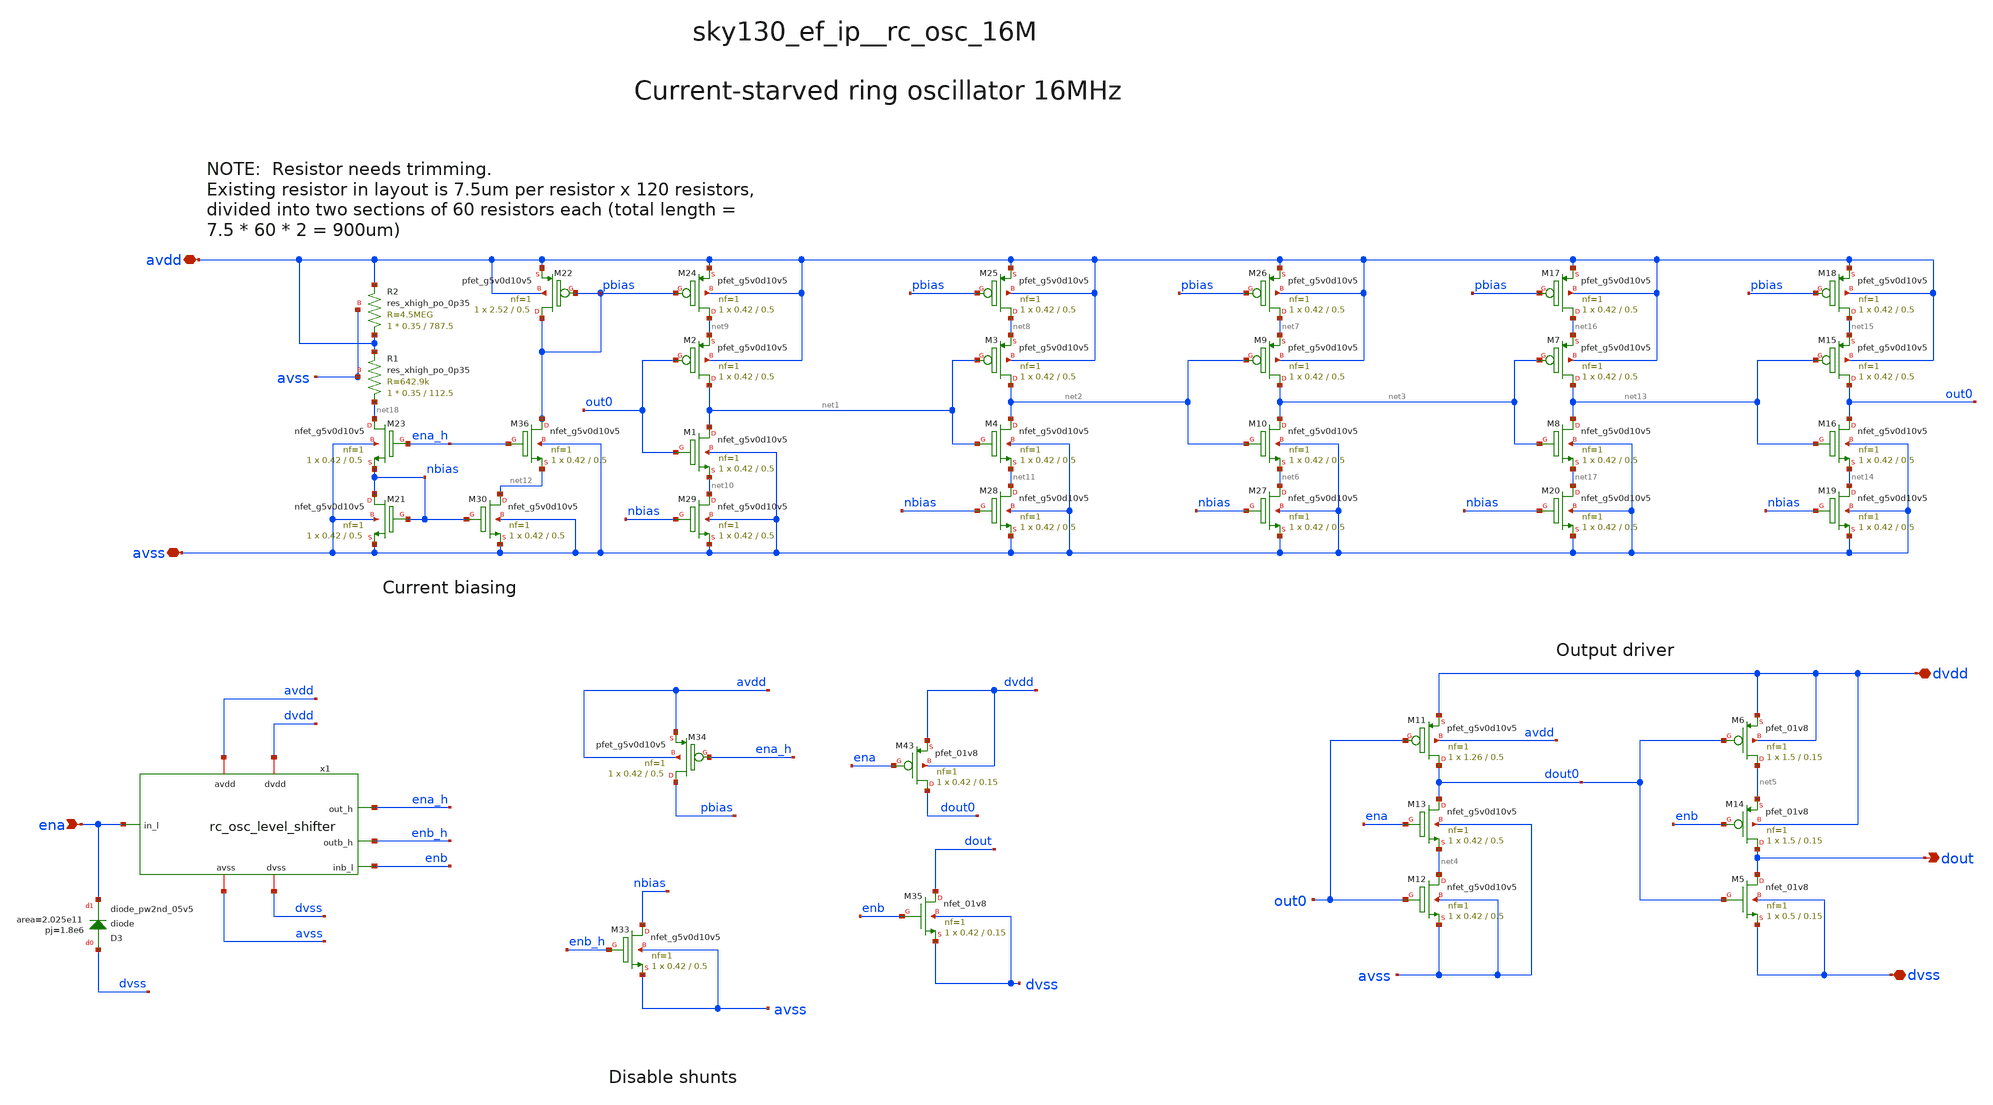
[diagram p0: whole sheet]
** sch_path: xschem/sky130_ef_ip__rc_osc_16M.sch
**.subckt sky130_ef_ip__rc_osc_16M avdd avss dvss dvdd ena dout
*.iopin avdd
*.iopin avss
*.iopin dvss
*.iopin dvdd
*.ipin ena
*.opin dout
XM1 net1 out0 net10 avss sky130_fd_pr__nfet_g5v0d10v5 L=0.5 W=0.42 nf=1 ad='int((nf+1)/2) * W/nf * 0.29'
+ as='int((nf+2)/2) * W/nf * 0.29' pd='2*int((nf+1)/2) * (W/nf + 0.29)' ps='2*int((nf+2)/2) * (W/nf + 0.29)'
+ nrd='0.29 / W' nrs='0.29 / W' sa=0 sb=0 sd=0 mult=1 m=1
XM2 net1 out0 net9 avdd sky130_fd_pr__pfet_g5v0d10v5 L=0.5 W=0.42 nf=1 ad='int((nf+1)/2) * W/nf * 0.29'
+ as='int((nf+2)/2) * W/nf * 0.29' pd='2*int((nf+1)/2) * (W/nf + 0.29)' ps='2*int((nf+2)/2) * (W/nf + 0.29)'
+ nrd='0.29 / W' nrs='0.29 / W' sa=0 sb=0 sd=0 mult=1 m=1
XM3 net2 net1 net8 avdd sky130_fd_pr__pfet_g5v0d10v5 L=0.5 W=0.42 nf=1 ad='int((nf+1)/2) * W/nf * 0.29'
+ as='int((nf+2)/2) * W/nf * 0.29' pd='2*int((nf+1)/2) * (W/nf + 0.29)' ps='2*int((nf+2)/2) * (W/nf + 0.29)'
+ nrd='0.29 / W' nrs='0.29 / W' sa=0 sb=0 sd=0 mult=1 m=1
XM4 net2 net1 net11 avss sky130_fd_pr__nfet_g5v0d10v5 L=0.5 W=0.42 nf=1 ad='int((nf+1)/2) * W/nf * 0.29'
+ as='int((nf+2)/2) * W/nf * 0.29' pd='2*int((nf+1)/2) * (W/nf + 0.29)' ps='2*int((nf+2)/2) * (W/nf + 0.29)'
+ nrd='0.29 / W' nrs='0.29 / W' sa=0 sb=0 sd=0 mult=1 m=1
XM5 dout dout0 dvss dvss sky130_fd_pr__nfet_01v8 L=0.15 W=0.5 nf=1 ad='int((nf+1)/2) * W/nf * 0.29' as='int((nf+2)/2) * W/nf * 0.29'
+ pd='2*int((nf+1)/2) * (W/nf + 0.29)' ps='2*int((nf+2)/2) * (W/nf + 0.29)' nrd='0.29 / W' nrs='0.29 / W'
+ sa=0 sb=0 sd=0 mult=1 m=1
XM6 net5 dout0 dvdd dvdd sky130_fd_pr__pfet_01v8 L=0.15 W=1.5 nf=1 ad='int((nf+1)/2) * W/nf * 0.29' as='int((nf+2)/2) * W/nf * 0.29'
+ pd='2*int((nf+1)/2) * (W/nf + 0.29)' ps='2*int((nf+2)/2) * (W/nf + 0.29)' nrd='0.29 / W' nrs='0.29 / W'
+ sa=0 sb=0 sd=0 mult=1 m=1
XM9 net3 net2 net7 avdd sky130_fd_pr__pfet_g5v0d10v5 L=0.5 W=0.42 nf=1 ad='int((nf+1)/2) * W/nf * 0.29'
+ as='int((nf+2)/2) * W/nf * 0.29' pd='2*int((nf+1)/2) * (W/nf + 0.29)' ps='2*int((nf+2)/2) * (W/nf + 0.29)'
+ nrd='0.29 / W' nrs='0.29 / W' sa=0 sb=0 sd=0 mult=1 m=1
XM10 net3 net2 net6 avss sky130_fd_pr__nfet_g5v0d10v5 L=0.5 W=0.42 nf=1 ad='int((nf+1)/2) * W/nf * 0.29'
+ as='int((nf+2)/2) * W/nf * 0.29' pd='2*int((nf+1)/2) * (W/nf + 0.29)' ps='2*int((nf+2)/2) * (W/nf + 0.29)'
+ nrd='0.29 / W' nrs='0.29 / W' sa=0 sb=0 sd=0 mult=1 m=1
XM11 dout0 out0 dvdd avdd sky130_fd_pr__pfet_g5v0d10v5 L=0.5 W=1.26 nf=1 ad='int((nf+1)/2) * W/nf * 0.29'
+ as='int((nf+2)/2) * W/nf * 0.29' pd='2*int((nf+1)/2) * (W/nf + 0.29)' ps='2*int((nf+2)/2) * (W/nf + 0.29)'
+ nrd='0.29 / W' nrs='0.29 / W' sa=0 sb=0 sd=0 mult=1 m=1
XM12 net4 out0 avss avss sky130_fd_pr__nfet_g5v0d10v5 L=0.5 W=0.42 nf=1 ad='int((nf+1)/2) * W/nf * 0.29'
+ as='int((nf+2)/2) * W/nf * 0.29' pd='2*int((nf+1)/2) * (W/nf + 0.29)' ps='2*int((nf+2)/2) * (W/nf + 0.29)'
+ nrd='0.29 / W' nrs='0.29 / W' sa=0 sb=0 sd=0 mult=1 m=1
XM13 dout0 ena net4 avss sky130_fd_pr__nfet_g5v0d10v5 L=0.5 W=0.42 nf=1 ad='int((nf+1)/2) * W/nf * 0.29'
+ as='int((nf+2)/2) * W/nf * 0.29' pd='2*int((nf+1)/2) * (W/nf + 0.29)' ps='2*int((nf+2)/2) * (W/nf + 0.29)'
+ nrd='0.29 / W' nrs='0.29 / W' sa=0 sb=0 sd=0 mult=1 m=1
XM24 net9 pbias avdd avdd sky130_fd_pr__pfet_g5v0d10v5 L=0.5 W=0.42 nf=1 ad='int((nf+1)/2) * W/nf * 0.29'
+ as='int((nf+2)/2) * W/nf * 0.29' pd='2*int((nf+1)/2) * (W/nf + 0.29)' ps='2*int((nf+2)/2) * (W/nf + 0.29)'
+ nrd='0.29 / W' nrs='0.29 / W' sa=0 sb=0 sd=0 mult=1 m=1
XM25 net8 pbias avdd avdd sky130_fd_pr__pfet_g5v0d10v5 L=0.5 W=0.42 nf=1 ad='int((nf+1)/2) * W/nf * 0.29'
+ as='int((nf+2)/2) * W/nf * 0.29' pd='2*int((nf+1)/2) * (W/nf + 0.29)' ps='2*int((nf+2)/2) * (W/nf + 0.29)'
+ nrd='0.29 / W' nrs='0.29 / W' sa=0 sb=0 sd=0 mult=1 m=1
XM26 net7 pbias avdd avdd sky130_fd_pr__pfet_g5v0d10v5 L=0.5 W=0.42 nf=1 ad='int((nf+1)/2) * W/nf * 0.29'
+ as='int((nf+2)/2) * W/nf * 0.29' pd='2*int((nf+1)/2) * (W/nf + 0.29)' ps='2*int((nf+2)/2) * (W/nf + 0.29)'
+ nrd='0.29 / W' nrs='0.29 / W' sa=0 sb=0 sd=0 mult=1 m=1
XM27 net6 nbias avss avss sky130_fd_pr__nfet_g5v0d10v5 L=0.5 W=0.42 nf=1 ad='int((nf+1)/2) * W/nf * 0.29'
+ as='int((nf+2)/2) * W/nf * 0.29' pd='2*int((nf+1)/2) * (W/nf + 0.29)' ps='2*int((nf+2)/2) * (W/nf + 0.29)'
+ nrd='0.29 / W' nrs='0.29 / W' sa=0 sb=0 sd=0 mult=1 m=1
XM28 net11 nbias avss avss sky130_fd_pr__nfet_g5v0d10v5 L=0.5 W=0.42 nf=1 ad='int((nf+1)/2) * W/nf * 0.29'
+ as='int((nf+2)/2) * W/nf * 0.29' pd='2*int((nf+1)/2) * (W/nf + 0.29)' ps='2*int((nf+2)/2) * (W/nf + 0.29)'
+ nrd='0.29 / W' nrs='0.29 / W' sa=0 sb=0 sd=0 mult=1 m=1
XM29 net10 nbias avss avss sky130_fd_pr__nfet_g5v0d10v5 L=0.5 W=0.42 nf=1 ad='int((nf+1)/2) * W/nf * 0.29'
+ as='int((nf+2)/2) * W/nf * 0.29' pd='2*int((nf+1)/2) * (W/nf + 0.29)' ps='2*int((nf+2)/2) * (W/nf + 0.29)'
+ nrd='0.29 / W' nrs='0.29 / W' sa=0 sb=0 sd=0 mult=1 m=1
XM21 nbias nbias avss avss sky130_fd_pr__nfet_g5v0d10v5 L=0.5 W=0.42 nf=1 ad='int((nf+1)/2) * W/nf * 0.29'
+ as='int((nf+2)/2) * W/nf * 0.29' pd='2*int((nf+1)/2) * (W/nf + 0.29)' ps='2*int((nf+2)/2) * (W/nf + 0.29)'
+ nrd='0.29 / W' nrs='0.29 / W' sa=0 sb=0 sd=0 mult=1 m=1
XM22 pbias pbias avdd avdd sky130_fd_pr__pfet_g5v0d10v5 L=0.5 W=2.52 nf=1 ad='int((nf+1)/2) * W/nf * 0.29'
+ as='int((nf+2)/2) * W/nf * 0.29' pd='2*int((nf+1)/2) * (W/nf + 0.29)' ps='2*int((nf+2)/2) * (W/nf + 0.29)'
+ nrd='0.29 / W' nrs='0.29 / W' sa=0 sb=0 sd=0 mult=1 m=1
XR1 net18 avdd avss sky130_fd_pr__res_xhigh_po_0p35 L=112.5 mult=1 m=1
XM23 net18 ena_h nbias avss sky130_fd_pr__nfet_g5v0d10v5 L=0.5 W=0.42 nf=1 ad='int((nf+1)/2) * W/nf * 0.29'
+ as='int((nf+2)/2) * W/nf * 0.29' pd='2*int((nf+1)/2) * (W/nf + 0.29)' ps='2*int((nf+2)/2) * (W/nf + 0.29)'
+ nrd='0.29 / W' nrs='0.29 / W' sa=0 sb=0 sd=0 mult=1 m=1
XM30 net12 nbias avss avss sky130_fd_pr__nfet_g5v0d10v5 L=0.5 W=0.42 nf=1 ad='int((nf+1)/2) * W/nf * 0.29'
+ as='int((nf+2)/2) * W/nf * 0.29' pd='2*int((nf+1)/2) * (W/nf + 0.29)' ps='2*int((nf+2)/2) * (W/nf + 0.29)'
+ nrd='0.29 / W' nrs='0.29 / W' sa=0 sb=0 sd=0 mult=1 m=1
XM33 nbias enb_h avss avss sky130_fd_pr__nfet_g5v0d10v5 L=0.5 W=0.42 nf=1 ad='int((nf+1)/2) * W/nf * 0.29'
+ as='int((nf+2)/2) * W/nf * 0.29' pd='2*int((nf+1)/2) * (W/nf + 0.29)' ps='2*int((nf+2)/2) * (W/nf + 0.29)'
+ nrd='0.29 / W' nrs='0.29 / W' sa=0 sb=0 sd=0 mult=1 m=1
XM34 pbias ena_h avdd avdd sky130_fd_pr__pfet_g5v0d10v5 L=0.5 W=0.42 nf=1 ad='int((nf+1)/2) * W/nf * 0.29'
+ as='int((nf+2)/2) * W/nf * 0.29' pd='2*int((nf+1)/2) * (W/nf + 0.29)' ps='2*int((nf+2)/2) * (W/nf + 0.29)'
+ nrd='0.29 / W' nrs='0.29 / W' sa=0 sb=0 sd=0 mult=1 m=1
XM36 pbias ena_h net12 avss sky130_fd_pr__nfet_g5v0d10v5 L=0.5 W=0.42 nf=1 ad='int((nf+1)/2) * W/nf * 0.29'
+ as='int((nf+2)/2) * W/nf * 0.29' pd='2*int((nf+1)/2) * (W/nf + 0.29)' ps='2*int((nf+2)/2) * (W/nf + 0.29)'
+ nrd='0.29 / W' nrs='0.29 / W' sa=0 sb=0 sd=0 mult=1 m=1
x1 dvdd ena_h avdd enb_h ena dvss avss enb rc_osc_level_shifter
XD3 dvss ena sky130_fd_pr__diode_pw2nd_05v5 area=2.025e11 pj=1.8e6
XM7 net13 net3 net16 avdd sky130_fd_pr__pfet_g5v0d10v5 L=0.5 W=0.42 nf=1 ad='int((nf+1)/2) * W/nf * 0.29'
+ as='int((nf+2)/2) * W/nf * 0.29' pd='2*int((nf+1)/2) * (W/nf + 0.29)' ps='2*int((nf+2)/2) * (W/nf + 0.29)'
+ nrd='0.29 / W' nrs='0.29 / W' sa=0 sb=0 sd=0 mult=1 m=1
XM8 net13 net3 net17 avss sky130_fd_pr__nfet_g5v0d10v5 L=0.5 W=0.42 nf=1 ad='int((nf+1)/2) * W/nf * 0.29'
+ as='int((nf+2)/2) * W/nf * 0.29' pd='2*int((nf+1)/2) * (W/nf + 0.29)' ps='2*int((nf+2)/2) * (W/nf + 0.29)'
+ nrd='0.29 / W' nrs='0.29 / W' sa=0 sb=0 sd=0 mult=1 m=1
XM15 out0 net13 net15 avdd sky130_fd_pr__pfet_g5v0d10v5 L=0.5 W=0.42 nf=1 ad='int((nf+1)/2) * W/nf * 0.29'
+ as='int((nf+2)/2) * W/nf * 0.29' pd='2*int((nf+1)/2) * (W/nf + 0.29)' ps='2*int((nf+2)/2) * (W/nf + 0.29)'
+ nrd='0.29 / W' nrs='0.29 / W' sa=0 sb=0 sd=0 mult=1 m=1
XM16 out0 net13 net14 avss sky130_fd_pr__nfet_g5v0d10v5 L=0.5 W=0.42 nf=1 ad='int((nf+1)/2) * W/nf * 0.29'
+ as='int((nf+2)/2) * W/nf * 0.29' pd='2*int((nf+1)/2) * (W/nf + 0.29)' ps='2*int((nf+2)/2) * (W/nf + 0.29)'
+ nrd='0.29 / W' nrs='0.29 / W' sa=0 sb=0 sd=0 mult=1 m=1
XM17 net16 pbias avdd avdd sky130_fd_pr__pfet_g5v0d10v5 L=0.5 W=0.42 nf=1 ad='int((nf+1)/2) * W/nf * 0.29'
+ as='int((nf+2)/2) * W/nf * 0.29' pd='2*int((nf+1)/2) * (W/nf + 0.29)' ps='2*int((nf+2)/2) * (W/nf + 0.29)'
+ nrd='0.29 / W' nrs='0.29 / W' sa=0 sb=0 sd=0 mult=1 m=1
XM18 net15 pbias avdd avdd sky130_fd_pr__pfet_g5v0d10v5 L=0.5 W=0.42 nf=1 ad='int((nf+1)/2) * W/nf * 0.29'
+ as='int((nf+2)/2) * W/nf * 0.29' pd='2*int((nf+1)/2) * (W/nf + 0.29)' ps='2*int((nf+2)/2) * (W/nf + 0.29)'
+ nrd='0.29 / W' nrs='0.29 / W' sa=0 sb=0 sd=0 mult=1 m=1
XM19 net14 nbias avss avss sky130_fd_pr__nfet_g5v0d10v5 L=0.5 W=0.42 nf=1 ad='int((nf+1)/2) * W/nf * 0.29'
+ as='int((nf+2)/2) * W/nf * 0.29' pd='2*int((nf+1)/2) * (W/nf + 0.29)' ps='2*int((nf+2)/2) * (W/nf + 0.29)'
+ nrd='0.29 / W' nrs='0.29 / W' sa=0 sb=0 sd=0 mult=1 m=1
XM20 net17 nbias avss avss sky130_fd_pr__nfet_g5v0d10v5 L=0.5 W=0.42 nf=1 ad='int((nf+1)/2) * W/nf * 0.29'
+ as='int((nf+2)/2) * W/nf * 0.29' pd='2*int((nf+1)/2) * (W/nf + 0.29)' ps='2*int((nf+2)/2) * (W/nf + 0.29)'
+ nrd='0.29 / W' nrs='0.29 / W' sa=0 sb=0 sd=0 mult=1 m=1
XM43 dout0 ena dvdd dvdd sky130_fd_pr__pfet_01v8 L=0.15 W=0.42 nf=1 ad='int((nf+1)/2) * W/nf * 0.29'
+ as='int((nf+2)/2) * W/nf * 0.29' pd='2*int((nf+1)/2) * (W/nf + 0.29)' ps='2*int((nf+2)/2) * (W/nf + 0.29)'
+ nrd='0.29 / W' nrs='0.29 / W' sa=0 sb=0 sd=0 mult=1 m=1
XM35 dout enb dvss dvss sky130_fd_pr__nfet_01v8 L=0.15 W=0.42 nf=1 ad='int((nf+1)/2) * W/nf * 0.29' as='int((nf+2)/2) * W/nf * 0.29'
+ pd='2*int((nf+1)/2) * (W/nf + 0.29)' ps='2*int((nf+2)/2) * (W/nf + 0.29)' nrd='0.29 / W' nrs='0.29 / W'
+ sa=0 sb=0 sd=0 mult=1 m=1
XM14 dout enb net5 dvdd sky130_fd_pr__pfet_01v8 L=0.15 W=1.5 nf=1 ad='int((nf+1)/2) * W/nf * 0.29' as='int((nf+2)/2) * W/nf * 0.29'
+ pd='2*int((nf+1)/2) * (W/nf + 0.29)' ps='2*int((nf+2)/2) * (W/nf + 0.29)' nrd='0.29 / W' nrs='0.29 / W'
+ sa=0 sb=0 sd=0 mult=1 m=1
XR2 avdd avdd avss sky130_fd_pr__res_xhigh_po_0p35 L=787.5 mult=1 m=1
**.ends
.end
